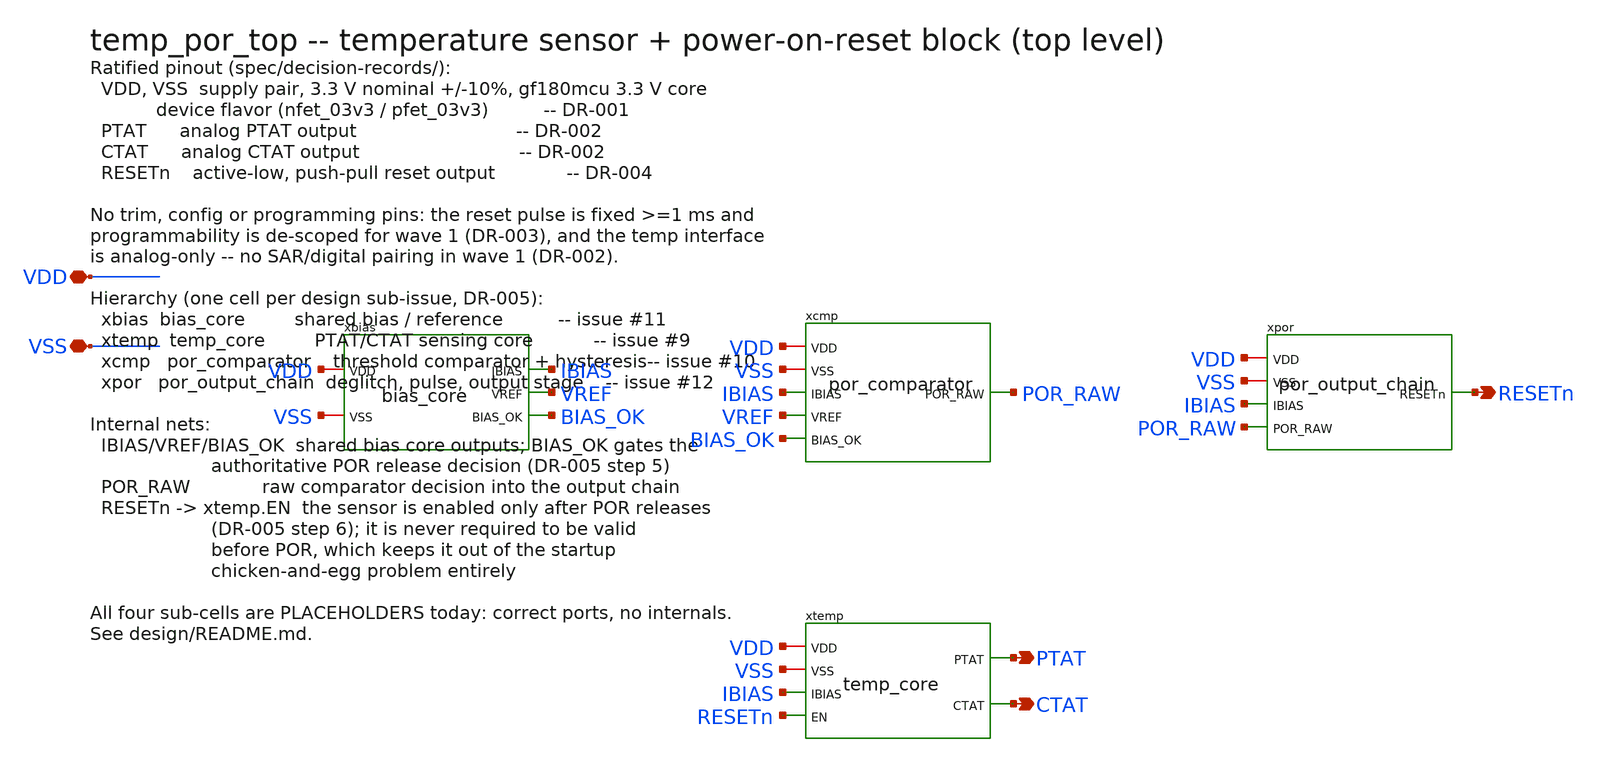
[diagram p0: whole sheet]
** sch_path: design/temp_por_top.sch
**.subckt temp_por_top VDD VSS PTAT CTAT RESETn
*.iopin VDD
*.iopin VSS
*.opin PTAT
*.opin CTAT
*.opin RESETn
xbias VDD VSS IBIAS VREF BIAS_OK bias_core
xtemp VDD VSS IBIAS RESETn PTAT CTAT temp_core
xcmp VDD VSS IBIAS VREF BIAS_OK POR_RAW por_comparator
xpor VDD VSS IBIAS POR_RAW RESETn por_output_chain
**.ends

* expanding   symbol:  bias_core.sym # of pins=5
** sym_path: design/bias_core.sym
** sch_path: design/bias_core.sch
.subckt bias_core VDD VSS IBIAS VREF BIAS_OK
*.iopin VDD
*.iopin VSS
*.opin IBIAS
*.opin VREF
*.opin BIAS_OK
XMP1 NA PG VDD VDD pfet_03v3 L=8u W=2u nf=1 ad='int((nf+1)/2) * W/nf * 0.18u' as='int((nf+2)/2) * W/nf * 0.18u'
+ pd='2*int((nf+1)/2) * (W/nf + 0.18u)' ps='2*int((nf+2)/2) * (W/nf + 0.18u)' nrd='0.18u / W' nrs='0.18u / W'
+ sa=0 sb=0 sd=0 m=1
XMP2 NB PG VDD VDD pfet_03v3 L=8u W=2u nf=1 ad='int((nf+1)/2) * W/nf * 0.18u' as='int((nf+2)/2) * W/nf * 0.18u'
+ pd='2*int((nf+1)/2) * (W/nf + 0.18u)' ps='2*int((nf+2)/2) * (W/nf + 0.18u)' nrd='0.18u / W' nrs='0.18u / W'
+ sa=0 sb=0 sd=0 m=1
XMP3 VREF PG VDD VDD pfet_03v3 L=8u W=2u nf=1 ad='int((nf+1)/2) * W/nf * 0.18u' as='int((nf+2)/2) * W/nf * 0.18u'
+ pd='2*int((nf+1)/2) * (W/nf + 0.18u)' ps='2*int((nf+2)/2) * (W/nf + 0.18u)' nrd='0.18u / W' nrs='0.18u / W'
+ sa=0 sb=0 sd=0 m=1
XMP4 IBIAS PG VDD VDD pfet_03v3 L=4u W=8u nf=1 ad='int((nf+1)/2) * W/nf * 0.18u' as='int((nf+2)/2) * W/nf * 0.18u'
+ pd='2*int((nf+1)/2) * (W/nf + 0.18u)' ps='2*int((nf+2)/2) * (W/nf + 0.18u)' nrd='0.18u / W' nrs='0.18u / W'
+ sa=0 sb=0 sd=0 m=1
XMT NT PG VDD VDD pfet_03v3 L=8u W=2u nf=1 ad='int((nf+1)/2) * W/nf * 0.18u' as='int((nf+2)/2) * W/nf * 0.18u'
+ pd='2*int((nf+1)/2) * (W/nf + 0.18u)' ps='2*int((nf+2)/2) * (W/nf + 0.18u)' nrd='0.18u / W' nrs='0.18u / W'
+ sa=0 sb=0 sd=0 m=1
XMS2P PG PB VDD VDD pfet_03v3 L=8u W=2u nf=1 ad='int((nf+1)/2) * W/nf * 0.18u' as='int((nf+2)/2) * W/nf * 0.18u'
+ pd='2*int((nf+1)/2) * (W/nf + 0.18u)' ps='2*int((nf+2)/2) * (W/nf + 0.18u)' nrd='0.18u / W' nrs='0.18u / W'
+ sa=0 sb=0 sd=0 m=1
XMBP PB PB VDD VDD pfet_03v3 L=8u W=1u nf=1 ad='int((nf+1)/2) * W/nf * 0.18u' as='int((nf+2)/2) * W/nf * 0.18u'
+ pd='2*int((nf+1)/2) * (W/nf + 0.18u)' ps='2*int((nf+2)/2) * (W/nf + 0.18u)' nrd='0.18u / W' nrs='0.18u / W'
+ sa=0 sb=0 sd=0 m=1
XMBN PB N1 VSS VSS nfet_03v3 L=8u W=1u nf=1 ad='int((nf+1)/2) * W/nf * 0.18u' as='int((nf+2)/2) * W/nf * 0.18u'
+ pd='2*int((nf+1)/2) * (W/nf + 0.18u)' ps='2*int((nf+2)/2) * (W/nf + 0.18u)' nrd='0.18u / W' nrs='0.18u / W'
+ sa=0 sb=0 sd=0 m=1
XQ1 VSS VSS NA pnp_10p00x10p00 m=1
XQ8A VSS VSS NC pnp_10p00x10p00 m=1
XQ8B VSS VSS NC pnp_10p00x10p00 m=1
XQ8C VSS VSS NC pnp_10p00x10p00 m=1
XQ8D VSS VSS NC pnp_10p00x10p00 m=1
XQ8E VSS VSS NC pnp_10p00x10p00 m=1
XQ8F VSS VSS NC pnp_10p00x10p00 m=1
XQ8G VSS VSS NC pnp_10p00x10p00 m=1
XQ8H VSS VSS NC pnp_10p00x10p00 m=1
XQR VSS VSS NRE pnp_10p00x10p00 m=1
XR1 NB NC VSS ppolyf_u_3k r_width=1u r_length=299u m=1
XR3 VREF NRE VSS ppolyf_u_3k r_width=1u r_length=3580u m=1
XMI1 N1 NA NT NT pfet_03v3 L=4u W=8u nf=1 ad='int((nf+1)/2) * W/nf * 0.18u' as='int((nf+2)/2) * W/nf * 0.18u'
+ pd='2*int((nf+1)/2) * (W/nf + 0.18u)' ps='2*int((nf+2)/2) * (W/nf + 0.18u)' nrd='0.18u / W' nrs='0.18u / W'
+ sa=0 sb=0 sd=0 m=1
XMI2 N2 NB NT NT pfet_03v3 L=4u W=8u nf=1 ad='int((nf+1)/2) * W/nf * 0.18u' as='int((nf+2)/2) * W/nf * 0.18u'
+ pd='2*int((nf+1)/2) * (W/nf + 0.18u)' ps='2*int((nf+2)/2) * (W/nf + 0.18u)' nrd='0.18u / W' nrs='0.18u / W'
+ sa=0 sb=0 sd=0 m=1
XML1 N1 N1 VSS VSS nfet_03v3 L=8u W=2u nf=1 ad='int((nf+1)/2) * W/nf * 0.18u' as='int((nf+2)/2) * W/nf * 0.18u'
+ pd='2*int((nf+1)/2) * (W/nf + 0.18u)' ps='2*int((nf+2)/2) * (W/nf + 0.18u)' nrd='0.18u / W' nrs='0.18u / W'
+ sa=0 sb=0 sd=0 m=1
XML2 N2 N1 VSS VSS nfet_03v3 L=8u W=2u nf=1 ad='int((nf+1)/2) * W/nf * 0.18u' as='int((nf+2)/2) * W/nf * 0.18u'
+ pd='2*int((nf+1)/2) * (W/nf + 0.18u)' ps='2*int((nf+2)/2) * (W/nf + 0.18u)' nrd='0.18u / W' nrs='0.18u / W'
+ sa=0 sb=0 sd=0 m=1
XMS2N PG N2 VSS VSS nfet_03v3 L=8u W=2u nf=1 ad='int((nf+1)/2) * W/nf * 0.18u' as='int((nf+2)/2) * W/nf * 0.18u'
+ pd='2*int((nf+1)/2) * (W/nf + 0.18u)' ps='2*int((nf+2)/2) * (W/nf + 0.18u)' nrd='0.18u / W' nrs='0.18u / W'
+ sa=0 sb=0 sd=0 m=1
XCC PG NZ cap_mim_2f0_m3m4_noshield c_width=45u c_length=45u m=1
XRZ NZ N2 VSS ppolyf_u_3k r_width=2u r_length=366u m=1
XMSU4 NK PG VDD VDD pfet_03v3 L=8u W=2u nf=1 ad='int((nf+1)/2) * W/nf * 0.18u' as='int((nf+2)/2) * W/nf * 0.18u'
+ pd='2*int((nf+1)/2) * (W/nf + 0.18u)' ps='2*int((nf+2)/2) * (W/nf + 0.18u)' nrd='0.18u / W' nrs='0.18u / W'
+ sa=0 sb=0 sd=0 m=1
XMNAT NK VSS NSD VSS nfet_06v0_nvt L=50u W=0.8u nf=1 ad='int((nf+1)/2) * W/nf * 0.18u' as='int((nf+2)/2) * W/nf * 0.18u'
+ pd='2*int((nf+1)/2) * (W/nf + 0.18u)' ps='2*int((nf+2)/2) * (W/nf + 0.18u)' nrd='0.18u / W' nrs='0.18u / W'
+ sa=0 sb=0 sd=0 m=16
XRDEG NSD VSS VSS ppolyf_u_3k r_width=1u r_length=1600u m=1
XMSU3 VSS NK PG PG pfet_03v3 L=2u W=1u nf=1 ad='int((nf+1)/2) * W/nf * 0.18u' as='int((nf+2)/2) * W/nf * 0.18u'
+ pd='2*int((nf+1)/2) * (W/nf + 0.18u)' ps='2*int((nf+2)/2) * (W/nf + 0.18u)' nrd='0.18u / W' nrs='0.18u / W'
+ sa=0 sb=0 sd=0 m=1
XMNKP NKB NK VDD VDD pfet_03v3 L=0.5u W=2u nf=1 ad='int((nf+1)/2) * W/nf * 0.18u' as='int((nf+2)/2) * W/nf * 0.18u'
+ pd='2*int((nf+1)/2) * (W/nf + 0.18u)' ps='2*int((nf+2)/2) * (W/nf + 0.18u)' nrd='0.18u / W' nrs='0.18u / W'
+ sa=0 sb=0 sd=0 m=1
XMNKN NKB NK VSS VSS nfet_03v3 L=0.5u W=1u nf=1 ad='int((nf+1)/2) * W/nf * 0.18u' as='int((nf+2)/2) * W/nf * 0.18u'
+ pd='2*int((nf+1)/2) * (W/nf + 0.18u)' ps='2*int((nf+2)/2) * (W/nf + 0.18u)' nrd='0.18u / W' nrs='0.18u / W'
+ sa=0 sb=0 sd=0 m=1
XMOKP NOK PG VDD VDD pfet_03v3 L=16u W=1u nf=1 ad='int((nf+1)/2) * W/nf * 0.18u' as='int((nf+2)/2) * W/nf * 0.18u'
+ pd='2*int((nf+1)/2) * (W/nf + 0.18u)' ps='2*int((nf+2)/2) * (W/nf + 0.18u)' nrd='0.18u / W' nrs='0.18u / W'
+ sa=0 sb=0 sd=0 m=1
XMOKD NOK NK VDD VDD pfet_03v3 L=0.5u W=2u nf=1 ad='int((nf+1)/2) * W/nf * 0.18u' as='int((nf+2)/2) * W/nf * 0.18u'
+ pd='2*int((nf+1)/2) * (W/nf + 0.18u)' ps='2*int((nf+2)/2) * (W/nf + 0.18u)' nrd='0.18u / W' nrs='0.18u / W'
+ sa=0 sb=0 sd=0 m=1
XMOKS NOK VREF VSS VSS nfet_03v3 L=8u W=1u nf=1 ad='int((nf+1)/2) * W/nf * 0.18u' as='int((nf+2)/2) * W/nf * 0.18u'
+ pd='2*int((nf+1)/2) * (W/nf + 0.18u)' ps='2*int((nf+2)/2) * (W/nf + 0.18u)' nrd='0.18u / W' nrs='0.18u / W'
+ sa=0 sb=0 sd=0 m=1
XMHD NHD VREF VDD VDD pfet_03v3 L=2u W=1u nf=1 ad='int((nf+1)/2) * W/nf * 0.18u' as='int((nf+2)/2) * W/nf * 0.18u'
+ pd='2*int((nf+1)/2) * (W/nf + 0.18u)' ps='2*int((nf+2)/2) * (W/nf + 0.18u)' nrd='0.18u / W' nrs='0.18u / W'
+ sa=0 sb=0 sd=0 m=1
XMHDL NHD N1 VSS VSS nfet_03v3 L=8u W=1u nf=1 ad='int((nf+1)/2) * W/nf * 0.18u' as='int((nf+2)/2) * W/nf * 0.18u'
+ pd='2*int((nf+1)/2) * (W/nf + 0.18u)' ps='2*int((nf+2)/2) * (W/nf + 0.18u)' nrd='0.18u / W' nrs='0.18u / W'
+ sa=0 sb=0 sd=0 m=1
XMHBP NHDB NHD VDD VDD pfet_03v3 L=0.5u W=2u nf=1 ad='int((nf+1)/2) * W/nf * 0.18u' as='int((nf+2)/2) * W/nf * 0.18u'
+ pd='2*int((nf+1)/2) * (W/nf + 0.18u)' ps='2*int((nf+2)/2) * (W/nf + 0.18u)' nrd='0.18u / W' nrs='0.18u / W'
+ sa=0 sb=0 sd=0 m=1
XMHBN NHDB NHD VSS VSS nfet_03v3 L=0.5u W=1u nf=1 ad='int((nf+1)/2) * W/nf * 0.18u' as='int((nf+2)/2) * W/nf * 0.18u'
+ pd='2*int((nf+1)/2) * (W/nf + 0.18u)' ps='2*int((nf+2)/2) * (W/nf + 0.18u)' nrd='0.18u / W' nrs='0.18u / W'
+ sa=0 sb=0 sd=0 m=1
XMNRP1 NRX NOK VDD VDD pfet_03v3 L=0.5u W=4u nf=1 ad='int((nf+1)/2) * W/nf * 0.18u' as='int((nf+2)/2) * W/nf * 0.18u'
+ pd='2*int((nf+1)/2) * (W/nf + 0.18u)' ps='2*int((nf+2)/2) * (W/nf + 0.18u)' nrd='0.18u / W' nrs='0.18u / W'
+ sa=0 sb=0 sd=0 m=1
XMNRP2 BIAS_OK NHDB NRX VDD pfet_03v3 L=0.5u W=4u nf=1 ad='int((nf+1)/2) * W/nf * 0.18u' as='int((nf+2)/2) * W/nf * 0.18u'
+ pd='2*int((nf+1)/2) * (W/nf + 0.18u)' ps='2*int((nf+2)/2) * (W/nf + 0.18u)' nrd='0.18u / W' nrs='0.18u / W'
+ sa=0 sb=0 sd=0 m=1
XMNRN1 BIAS_OK NOK VSS VSS nfet_03v3 L=0.5u W=2u nf=1 ad='int((nf+1)/2) * W/nf * 0.18u' as='int((nf+2)/2) * W/nf * 0.18u'
+ pd='2*int((nf+1)/2) * (W/nf + 0.18u)' ps='2*int((nf+2)/2) * (W/nf + 0.18u)' nrd='0.18u / W' nrs='0.18u / W'
+ sa=0 sb=0 sd=0 m=1
XMNRN2 BIAS_OK NHDB VSS VSS nfet_03v3 L=0.5u W=2u nf=1 ad='int((nf+1)/2) * W/nf * 0.18u' as='int((nf+2)/2) * W/nf * 0.18u'
+ pd='2*int((nf+1)/2) * (W/nf + 0.18u)' ps='2*int((nf+2)/2) * (W/nf + 0.18u)' nrd='0.18u / W' nrs='0.18u / W'
+ sa=0 sb=0 sd=0 m=1
XMOKZ BIAS_OK NKB VSS VSS nfet_03v3 L=0.5u W=16u nf=1 ad='int((nf+1)/2) * W/nf * 0.18u' as='int((nf+2)/2) * W/nf * 0.18u'
+ pd='2*int((nf+1)/2) * (W/nf + 0.18u)' ps='2*int((nf+2)/2) * (W/nf + 0.18u)' nrd='0.18u / W' nrs='0.18u / W'
+ sa=0 sb=0 sd=0 m=1
.ends


* expanding   symbol:  temp_core.sym # of pins=6
** sym_path: design/temp_core.sym
** sch_path: design/temp_core.sch
.subckt temp_core VDD VSS IBIAS EN PTAT CTAT
*.iopin VDD
*.iopin VSS
*.ipin IBIAS
*.ipin EN
*.opin PTAT
*.opin CTAT
Rplaceholder_ptat PTAT VSS 1T m=1
Rplaceholder_ctat CTAT VSS 1T m=1
**** begin user architecture code

* PLACEHOLDER: temp_core has no internals yet -- they land with issue #9.
* The Rplaceholder_* devices in this cell are 1 Tohm terminations, not
* design content: they exist only so this stub is ERC-clean and DC-solvable.
* Nothing in this cell may be cited as simulation evidence.

**** end user architecture code
.ends


* expanding   symbol:  por_comparator.sym # of pins=6
** sym_path: design/por_comparator.sym
** sch_path: design/por_comparator.sch
.subckt por_comparator VDD VSS IBIAS VREF BIAS_OK POR_RAW
*.iopin VDD
*.iopin VSS
*.ipin IBIAS
*.ipin VREF
*.ipin BIAS_OK
*.opin POR_RAW
Rplaceholder_por_raw POR_RAW VSS 1T m=1
**** begin user architecture code

* PLACEHOLDER: por_comparator has no internals yet -- they land with issue #10.
* The Rplaceholder_* devices in this cell are 1 Tohm terminations, not
* design content: they exist only so this stub is ERC-clean and DC-solvable.
* Nothing in this cell may be cited as simulation evidence.

**** end user architecture code
.ends


* expanding   symbol:  por_output_chain.sym # of pins=5
** sym_path: design/por_output_chain.sym
** sch_path: design/por_output_chain.sch
.subckt por_output_chain VDD VSS IBIAS POR_RAW RESETn
*.iopin VDD
*.iopin VSS
*.ipin IBIAS
*.ipin POR_RAW
*.opin RESETn
XMBD IBIAS IBIAS VSS VSS nfet_03v3 L=4u W=4u nf=1 ad='int((nf+1)/2) * W/nf * 0.18u' as='int((nf+2)/2) * W/nf * 0.18u'
+ pd='2*int((nf+1)/2) * (W/nf + 0.18u)' ps='2*int((nf+2)/2) * (W/nf + 0.18u)' nrd='0.18u / W' nrs='0.18u / W'
+ sa=0 sb=0 sd=0 m=1
XMN1 PDN IBIAS VSS VSS nfet_03v3 L=25u W=0.5u nf=1 ad='int((nf+1)/2) * W/nf * 0.18u' as='int((nf+2)/2) * W/nf * 0.18u'
+ pd='2*int((nf+1)/2) * (W/nf + 0.18u)' ps='2*int((nf+2)/2) * (W/nf + 0.18u)' nrd='0.18u / W' nrs='0.18u / W'
+ sa=0 sb=0 sd=0 m=1
XMPD PDN PDN VDD VDD pfet_03v3 L=10u W=2u nf=1 ad='int((nf+1)/2) * W/nf * 0.18u' as='int((nf+2)/2) * W/nf * 0.18u'
+ pd='2*int((nf+1)/2) * (W/nf + 0.18u)' ps='2*int((nf+2)/2) * (W/nf + 0.18u)' nrd='0.18u / W' nrs='0.18u / W'
+ sa=0 sb=0 sd=0 m=1
XMP2 NDL PDN VDD VDD pfet_03v3 L=10u W=2u nf=1 ad='int((nf+1)/2) * W/nf * 0.18u' as='int((nf+2)/2) * W/nf * 0.18u'
+ pd='2*int((nf+1)/2) * (W/nf + 0.18u)' ps='2*int((nf+2)/2) * (W/nf + 0.18u)' nrd='0.18u / W' nrs='0.18u / W'
+ sa=0 sb=0 sd=0 m=1
XMND NDL NDL VSS VSS nfet_03v3 L=10u W=2u nf=1 ad='int((nf+1)/2) * W/nf * 0.18u' as='int((nf+2)/2) * W/nf * 0.18u'
+ pd='2*int((nf+1)/2) * (W/nf + 0.18u)' ps='2*int((nf+2)/2) * (W/nf + 0.18u)' nrd='0.18u / W' nrs='0.18u / W'
+ sa=0 sb=0 sd=0 m=1
XMDGPT NDGP PDN VDD VDD pfet_03v3 L=10u W=10u nf=1 ad='int((nf+1)/2) * W/nf * 0.18u' as='int((nf+2)/2) * W/nf * 0.18u'
+ pd='2*int((nf+1)/2) * (W/nf + 0.18u)' ps='2*int((nf+2)/2) * (W/nf + 0.18u)' nrd='0.18u / W' nrs='0.18u / W'
+ sa=0 sb=0 sd=0 m=1
XMDGPI NDG POR_RAW NDGP VDD pfet_03v3 L=0.5u W=1u nf=1 ad='int((nf+1)/2) * W/nf * 0.18u' as='int((nf+2)/2) * W/nf * 0.18u'
+ pd='2*int((nf+1)/2) * (W/nf + 0.18u)' ps='2*int((nf+2)/2) * (W/nf + 0.18u)' nrd='0.18u / W' nrs='0.18u / W'
+ sa=0 sb=0 sd=0 m=1
XMDGNI NDG POR_RAW NDGN VSS nfet_03v3 L=0.5u W=1u nf=1 ad='int((nf+1)/2) * W/nf * 0.18u' as='int((nf+2)/2) * W/nf * 0.18u'
+ pd='2*int((nf+1)/2) * (W/nf + 0.18u)' ps='2*int((nf+2)/2) * (W/nf + 0.18u)' nrd='0.18u / W' nrs='0.18u / W'
+ sa=0 sb=0 sd=0 m=1
XMDGNT NDGN NDL VSS VSS nfet_03v3 L=10u W=10u nf=1 ad='int((nf+1)/2) * W/nf * 0.18u' as='int((nf+2)/2) * W/nf * 0.18u'
+ pd='2*int((nf+1)/2) * (W/nf + 0.18u)' ps='2*int((nf+2)/2) * (W/nf + 0.18u)' nrd='0.18u / W' nrs='0.18u / W'
+ sa=0 sb=0 sd=0 m=1
XCDG NDG VSS cap_mim_2f0_m3m4_noshield c_width=11u c_length=11u m=1
XMG1P PGDG NDG VDD VDD pfet_03v3 L=2u W=0.5u nf=1 ad='int((nf+1)/2) * W/nf * 0.18u' as='int((nf+2)/2) * W/nf * 0.18u'
+ pd='2*int((nf+1)/2) * (W/nf + 0.18u)' ps='2*int((nf+2)/2) * (W/nf + 0.18u)' nrd='0.18u / W' nrs='0.18u / W'
+ sa=0 sb=0 sd=0 m=1
XMG1N PGDG NDG VSS VSS nfet_03v3 L=0.5u W=2u nf=1 ad='int((nf+1)/2) * W/nf * 0.18u' as='int((nf+2)/2) * W/nf * 0.18u'
+ pd='2*int((nf+1)/2) * (W/nf + 0.18u)' ps='2*int((nf+2)/2) * (W/nf + 0.18u)' nrd='0.18u / W' nrs='0.18u / W'
+ sa=0 sb=0 sd=0 m=1
XMG2P PGDGB PGDG VDD VDD pfet_03v3 L=0.5u W=2u nf=1 ad='int((nf+1)/2) * W/nf * 0.18u' as='int((nf+2)/2) * W/nf * 0.18u'
+ pd='2*int((nf+1)/2) * (W/nf + 0.18u)' ps='2*int((nf+2)/2) * (W/nf + 0.18u)' nrd='0.18u / W' nrs='0.18u / W'
+ sa=0 sb=0 sd=0 m=1
XMG2N PGDGB PGDG VSS VSS nfet_03v3 L=2u W=0.5u nf=1 ad='int((nf+1)/2) * W/nf * 0.18u' as='int((nf+2)/2) * W/nf * 0.18u'
+ pd='2*int((nf+1)/2) * (W/nf + 0.18u)' ps='2*int((nf+2)/2) * (W/nf + 0.18u)' nrd='0.18u / W' nrs='0.18u / W'
+ sa=0 sb=0 sd=0 m=1
XMPT NTS PDN VDD VDD pfet_03v3 L=10u W=0.5u nf=1 ad='int((nf+1)/2) * W/nf * 0.18u' as='int((nf+2)/2) * W/nf * 0.18u'
+ pd='2*int((nf+1)/2) * (W/nf + 0.18u)' ps='2*int((nf+2)/2) * (W/nf + 0.18u)' nrd='0.18u / W' nrs='0.18u / W'
+ sa=0 sb=0 sd=0 m=1
XMTSW TIM PGDGB NTS VDD pfet_03v3 L=1u W=2u nf=1 ad='int((nf+1)/2) * W/nf * 0.18u' as='int((nf+2)/2) * W/nf * 0.18u'
+ pd='2*int((nf+1)/2) * (W/nf + 0.18u)' ps='2*int((nf+2)/2) * (W/nf + 0.18u)' nrd='0.18u / W' nrs='0.18u / W'
+ sa=0 sb=0 sd=0 m=1
XMDIS TIM PGDGB VSS VSS nfet_03v3 L=1u W=1u nf=1 ad='int((nf+1)/2) * W/nf * 0.18u' as='int((nf+2)/2) * W/nf * 0.18u'
+ pd='2*int((nf+1)/2) * (W/nf + 0.18u)' ps='2*int((nf+2)/2) * (W/nf + 0.18u)' nrd='0.18u / W' nrs='0.18u / W'
+ sa=0 sb=0 sd=0 m=1
XCTIM TIM VSS cap_mim_2f0_m3m4_noshield c_width=28u c_length=28u m=4
XMDAPI ND1 TIM VDD VDD pfet_03v3 L=1u W=2u nf=1 ad='int((nf+1)/2) * W/nf * 0.18u' as='int((nf+2)/2) * W/nf * 0.18u'
+ pd='2*int((nf+1)/2) * (W/nf + 0.18u)' ps='2*int((nf+2)/2) * (W/nf + 0.18u)' nrd='0.18u / W' nrs='0.18u / W'
+ sa=0 sb=0 sd=0 m=1
XMDANT ND1 NDL VSS VSS nfet_03v3 L=10u W=0.5u nf=1 ad='int((nf+1)/2) * W/nf * 0.18u' as='int((nf+2)/2) * W/nf * 0.18u'
+ pd='2*int((nf+1)/2) * (W/nf + 0.18u)' ps='2*int((nf+2)/2) * (W/nf + 0.18u)' nrd='0.18u / W' nrs='0.18u / W'
+ sa=0 sb=0 sd=0 m=1
XMDBNI TRIP ND1 VSS VSS nfet_03v3 L=1u W=1u nf=1 ad='int((nf+1)/2) * W/nf * 0.18u' as='int((nf+2)/2) * W/nf * 0.18u'
+ pd='2*int((nf+1)/2) * (W/nf + 0.18u)' ps='2*int((nf+2)/2) * (W/nf + 0.18u)' nrd='0.18u / W' nrs='0.18u / W'
+ sa=0 sb=0 sd=0 m=1
XMDBPT TRIP PDN VDD VDD pfet_03v3 L=10u W=0.5u nf=1 ad='int((nf+1)/2) * W/nf * 0.18u' as='int((nf+2)/2) * W/nf * 0.18u'
+ pd='2*int((nf+1)/2) * (W/nf + 0.18u)' ps='2*int((nf+2)/2) * (W/nf + 0.18u)' nrd='0.18u / W' nrs='0.18u / W'
+ sa=0 sb=0 sd=0 m=1
XMRLK ND1 RESETn VSS VSS nfet_03v3 L=1u W=1u nf=1 ad='int((nf+1)/2) * W/nf * 0.18u' as='int((nf+2)/2) * W/nf * 0.18u'
+ pd='2*int((nf+1)/2) * (W/nf + 0.18u)' ps='2*int((nf+2)/2) * (W/nf + 0.18u)' nrd='0.18u / W' nrs='0.18u / W'
+ sa=0 sb=0 sd=0 m=1
XMNAP1 RSTB TRIP VDD VDD pfet_03v3 L=0.5u W=4u nf=1 ad='int((nf+1)/2) * W/nf * 0.18u' as='int((nf+2)/2) * W/nf * 0.18u'
+ pd='2*int((nf+1)/2) * (W/nf + 0.18u)' ps='2*int((nf+2)/2) * (W/nf + 0.18u)' nrd='0.18u / W' nrs='0.18u / W'
+ sa=0 sb=0 sd=0 m=1
XMNAP2 RSTB PGDG VDD VDD pfet_03v3 L=0.5u W=4u nf=1 ad='int((nf+1)/2) * W/nf * 0.18u' as='int((nf+2)/2) * W/nf * 0.18u'
+ pd='2*int((nf+1)/2) * (W/nf + 0.18u)' ps='2*int((nf+2)/2) * (W/nf + 0.18u)' nrd='0.18u / W' nrs='0.18u / W'
+ sa=0 sb=0 sd=0 m=1
XMNAN1 RSTB TRIP NNAND VSS nfet_03v3 L=0.5u W=2u nf=1 ad='int((nf+1)/2) * W/nf * 0.18u' as='int((nf+2)/2) * W/nf * 0.18u'
+ pd='2*int((nf+1)/2) * (W/nf + 0.18u)' ps='2*int((nf+2)/2) * (W/nf + 0.18u)' nrd='0.18u / W' nrs='0.18u / W'
+ sa=0 sb=0 sd=0 m=1
XMNAN2 NNAND PGDG VSS VSS nfet_03v3 L=0.5u W=2u nf=1 ad='int((nf+1)/2) * W/nf * 0.18u' as='int((nf+2)/2) * W/nf * 0.18u'
+ pd='2*int((nf+1)/2) * (W/nf + 0.18u)' ps='2*int((nf+2)/2) * (W/nf + 0.18u)' nrd='0.18u / W' nrs='0.18u / W'
+ sa=0 sb=0 sd=0 m=1
XMAST RSTB RESETn VDD VDD pfet_03v3 L=10u W=0.5u nf=1 ad='int((nf+1)/2) * W/nf * 0.18u' as='int((nf+2)/2) * W/nf * 0.18u'
+ pd='2*int((nf+1)/2) * (W/nf + 0.18u)' ps='2*int((nf+2)/2) * (W/nf + 0.18u)' nrd='0.18u / W' nrs='0.18u / W'
+ sa=0 sb=0 sd=0 m=1
XMOP RESETn RSTB VDD VDD pfet_03v3 L=1u W=1u nf=1 ad='int((nf+1)/2) * W/nf * 0.18u' as='int((nf+2)/2) * W/nf * 0.18u'
+ pd='2*int((nf+1)/2) * (W/nf + 0.18u)' ps='2*int((nf+2)/2) * (W/nf + 0.18u)' nrd='0.18u / W' nrs='0.18u / W'
+ sa=0 sb=0 sd=0 m=1
XMON RESETn RSTB VSS VSS nfet_03v3 L=0.5u W=10u nf=1 ad='int((nf+1)/2) * W/nf * 0.18u' as='int((nf+2)/2) * W/nf * 0.18u'
+ pd='2*int((nf+1)/2) * (W/nf + 0.18u)' ps='2*int((nf+2)/2) * (W/nf + 0.18u)' nrd='0.18u / W' nrs='0.18u / W'
+ sa=0 sb=0 sd=0 m=1
.ends

.end
